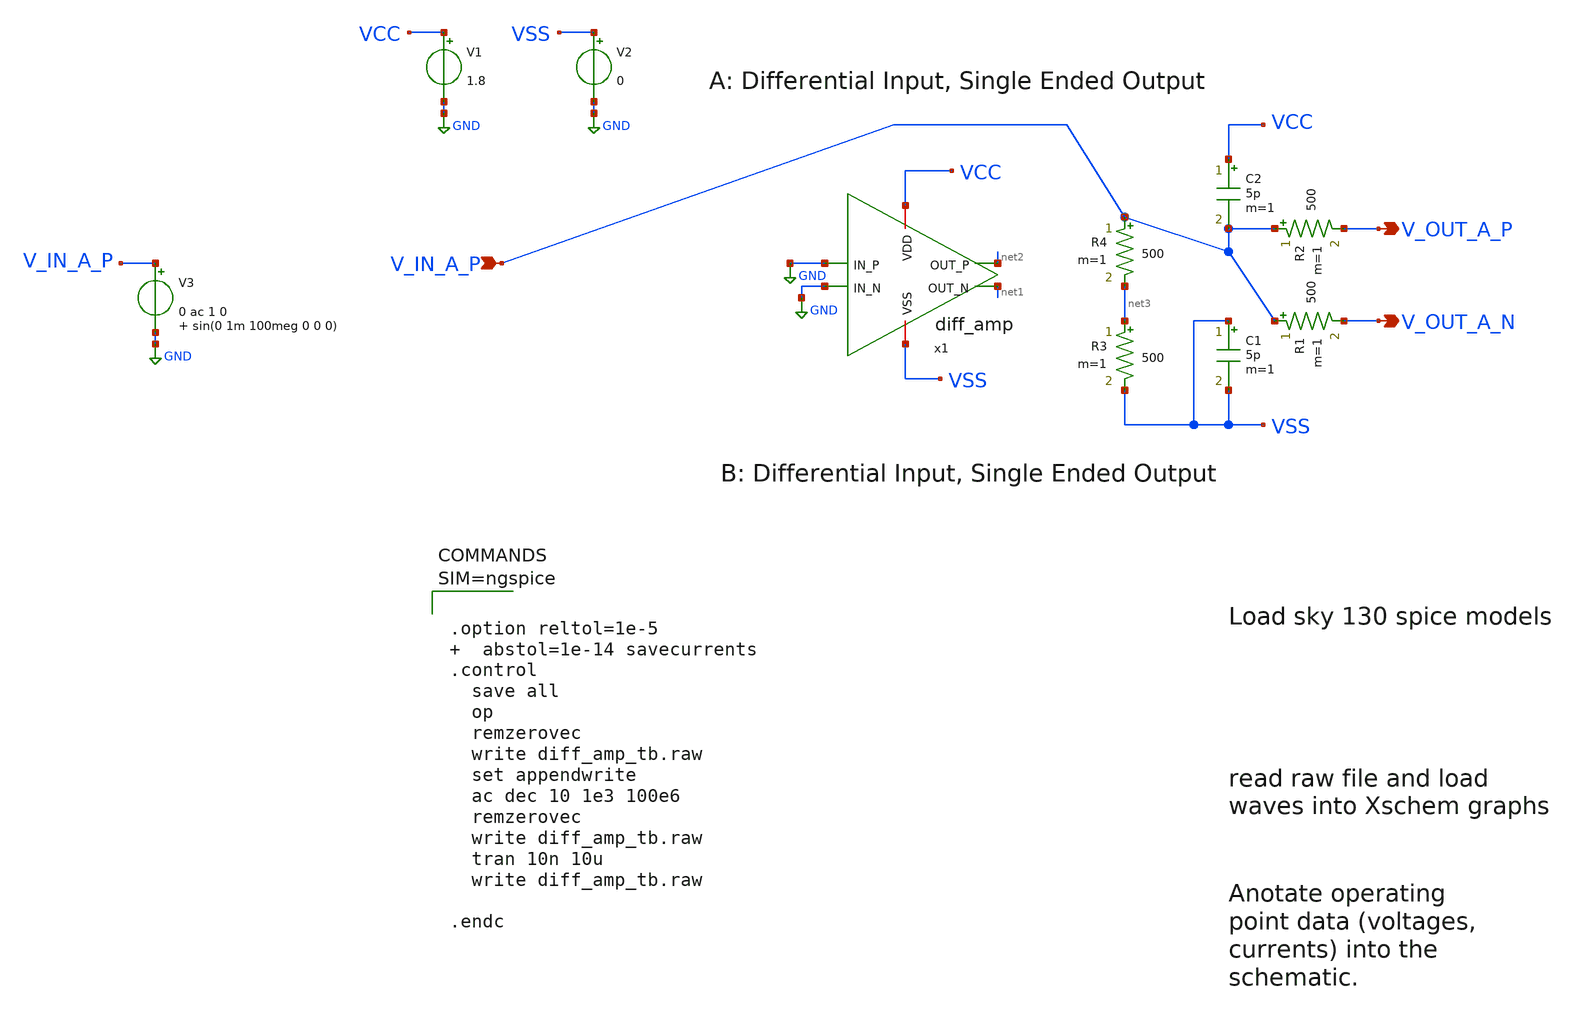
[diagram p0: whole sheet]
** sch_path: xschem/diff_amp_tb.sch
**.subckt diff_amp_tb V_IN_A_P V_OUT_A_N V_OUT_A_P
*.ipin V_IN_A_P
*.opin V_OUT_A_N
*.opin V_OUT_A_P
x1 VCC VSS GND net2 net1 GND diff_amp
V1 VCC GND 1.8
V2 VSS GND 0
R1 V_IN_A_P V_OUT_A_N 500 m=1
C1 VSS VSS 5p m=1
R2 V_IN_A_P V_OUT_A_P 500 m=1
C2 VCC V_IN_A_P 5p m=1
V3 V_IN_A_P GND 0 ac 1 0 sin(0 1m 100meg 0 0 0)
R3 net3 VSS 500 m=1
R4 V_IN_A_P net3 500 m=1
**** begin user architecture code

** opencircuitdesign pdks install
.lib $::SKYWATER_MODELS/sky130.lib.spice tt





.option reltol=1e-5   abstol=1e-14 savecurrents
.control
  save all
  op
  remzerovec
  write diff_amp_tb.raw
  set appendwrite
  ac dec 10 1e3 100e6
  remzerovec
  write diff_amp_tb.raw
  tran 10n 10u
  write diff_amp_tb.raw

.endc



**** end user architecture code
**.ends

* expanding   symbol:  diff_amp.sym # of pins=6
** sym_path: xschem/diff_amp.sym
** sch_path: xschem/diff_amp.sch
.subckt diff_amp VDD VSS IN_N OUT_P OUT_N IN_P
*.iopin VDD
*.iopin VSS
*.ipin IN_N
*.ipin IN_P
*.opin OUT_P
*.opin OUT_N
XM3 VX net1 VSS VSS sky130_fd_pr__nfet_01v8 L=2 W=4 nf=4 ad='int((nf+1)/2) * W/nf * 0.29' as='int((nf+2)/2) * W/nf * 0.29'
+ pd='2*int((nf+1)/2) * (W/nf + 0.29)' ps='2*int((nf+2)/2) * (W/nf + 0.29)' nrd='0.29 / W' nrs='0.29 / W'
+ sa=0 sb=0 sd=0 mult=1 m=1
XM6 net1 net1 VSS VSS sky130_fd_pr__nfet_01v8 L=2 W=4 nf=4 ad='int((nf+1)/2) * W/nf * 0.29' as='int((nf+2)/2) * W/nf * 0.29'
+ pd='2*int((nf+1)/2) * (W/nf + 0.29)' ps='2*int((nf+2)/2) * (W/nf + 0.29)' nrd='0.29 / W' nrs='0.29 / W'
+ sa=0 sb=0 sd=0 mult=1 m=1
XR1 net1 VDD VSS sky130_fd_pr__res_xhigh_po_0p35 L=2.8 mult=1 m=1
XM2 OUT_P IN_P VX VSS sky130_fd_pr__nfet_01v8_lvt L=0.5 W=2.5 nf=1 ad='int((nf+1)/2) * W/nf * 0.29' as='int((nf+2)/2) * W/nf * 0.29'
+ pd='2*int((nf+1)/2) * (W/nf + 0.29)' ps='2*int((nf+2)/2) * (W/nf + 0.29)' nrd='0.29 / W' nrs='0.29 / W'
+ sa=0 sb=0 sd=0 mult=1 m=1
XM1 OUT_N IN_N VX VSS sky130_fd_pr__nfet_01v8_lvt L=0.5 W=2.5 nf=1 ad='int((nf+1)/2) * W/nf * 0.29' as='int((nf+2)/2) * W/nf * 0.29'
+ pd='2*int((nf+1)/2) * (W/nf + 0.29)' ps='2*int((nf+2)/2) * (W/nf + 0.29)' nrd='0.29 / W' nrs='0.29 / W'
+ sa=0 sb=0 sd=0 mult=1 m=1
XM4 OUT_P OUT_P VDD VDD sky130_fd_pr__pfet_01v8_lvt L=2 W=6 nf=6 ad='int((nf+1)/2) * W/nf * 0.29' as='int((nf+2)/2) * W/nf * 0.29'
+ pd='2*int((nf+1)/2) * (W/nf + 0.29)' ps='2*int((nf+2)/2) * (W/nf + 0.29)' nrd='0.29 / W' nrs='0.29 / W'
+ sa=0 sb=0 sd=0 mult=1 m=1
XM5 OUT_N OUT_P VDD VDD sky130_fd_pr__pfet_01v8_lvt L=2 W=6 nf=6 ad='int((nf+1)/2) * W/nf * 0.29' as='int((nf+2)/2) * W/nf * 0.29'
+ pd='2*int((nf+1)/2) * (W/nf + 0.29)' ps='2*int((nf+2)/2) * (W/nf + 0.29)' nrd='0.29 / W' nrs='0.29 / W'
+ sa=0 sb=0 sd=0 mult=1 m=1
.ends

.GLOBAL GND
.end
